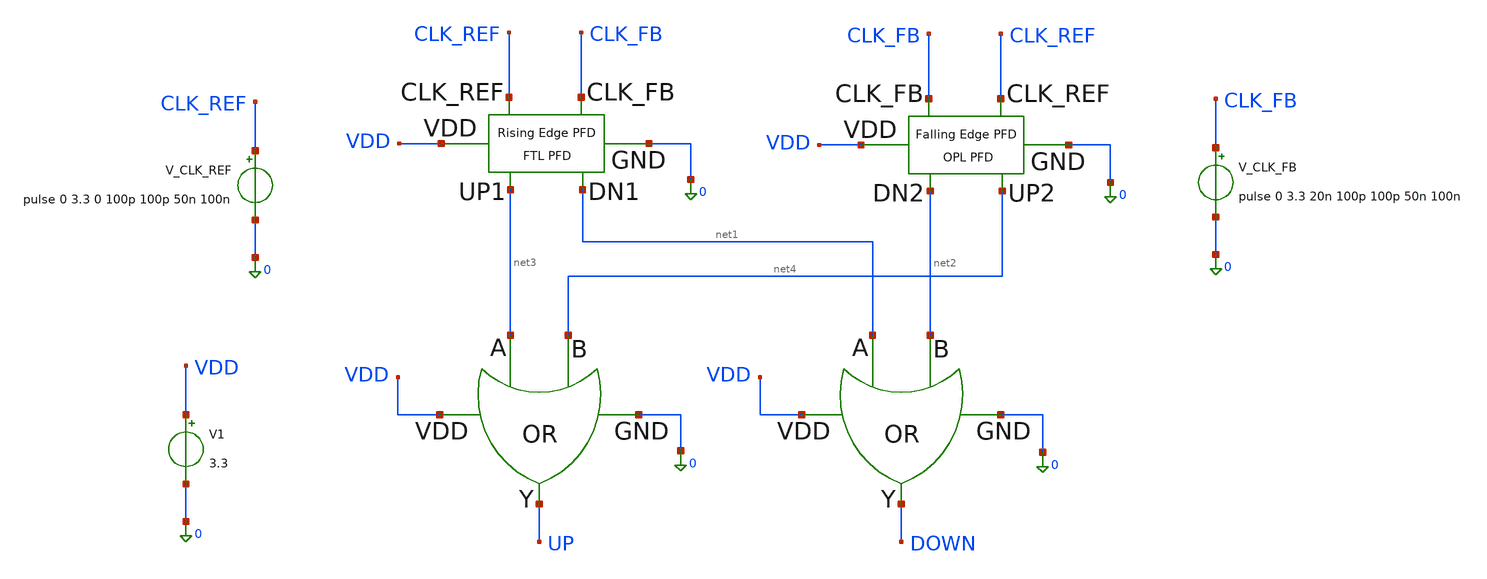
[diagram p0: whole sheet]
** sch_path: PFD/DELD_PFD.sch
**.subckt DELD_PFD
x1 0 net1 net2 VDD DOWN OR
x2 0 net3 net4 VDD UP OR
x3 net1 net3 CLK_FB CLK_REF VDD 0 FTL_PFD
x4 net4 net2 CLK_REF CLK_FB VDD 0 OPL_PFD
V1 VDD 0 3.3
.save i(v1)
V_CLK_REF CLK_REF 0 pulse 0 3.3 0 100p 100p 50n 100n
.save i(v_clk_ref)
V_CLK_FB CLK_FB 0 pulse 0 3.3 20n 100p 100p 50n 100n
.save i(v_clk_fb)
**.ends

* expanding   symbol:  OR.sym # of pins=5
** sym_path: PFD/OR.sym
** sch_path: PFD/OR.sch
.subckt OR GND A B VDD Y
*.opin Y
*.ipin GND
*.ipin VDD
*.ipin A
*.ipin B
XM3 net2 A GND GND nfet_03v3 L=0.28u W=0.22u nf=1 ad='int((nf+1)/2) * W/nf * 0.18u' as='int((nf+2)/2) * W/nf * 0.18u'
+ pd='2*int((nf+1)/2) * (W/nf + 0.18u)' ps='2*int((nf+2)/2) * (W/nf + 0.18u)' nrd='0.18u / W' nrs='0.18u / W'
+ sa=0 sb=0 sd=0 m=1
XM2 net1 A net3 VDD pfet_03v3 L=0.28u W=0.22u nf=1 ad='int((nf+1)/2) * W/nf * 0.18u' as='int((nf+2)/2) * W/nf * 0.18u'
+ pd='2*int((nf+1)/2) * (W/nf + 0.18u)' ps='2*int((nf+2)/2) * (W/nf + 0.18u)' nrd='0.18u / W' nrs='0.18u / W'
+ sa=0 sb=0 sd=0 m=3
XM4 net2 B net1 net4 pfet_03v3 L=0.28u W=0.22u nf=1 ad='int((nf+1)/2) * W/nf * 0.18u' as='int((nf+2)/2) * W/nf * 0.18u'
+ pd='2*int((nf+1)/2) * (W/nf + 0.18u)' ps='2*int((nf+2)/2) * (W/nf + 0.18u)' nrd='0.18u / W' nrs='0.18u / W'
+ sa=0 sb=0 sd=0 m=3
XM1 net2 B GND GND nfet_03v3 L=0.28u W=0.22u nf=1 ad='int((nf+1)/2) * W/nf * 0.18u' as='int((nf+2)/2) * W/nf * 0.18u'
+ pd='2*int((nf+1)/2) * (W/nf + 0.18u)' ps='2*int((nf+2)/2) * (W/nf + 0.18u)' nrd='0.18u / W' nrs='0.18u / W'
+ sa=0 sb=0 sd=0 m=1
XM29 Y net2 VDD VDD pfet_03v3 L=0.28u W=0.22u nf=1 ad='int((nf+1)/2) * W/nf * 0.18u' as='int((nf+2)/2) * W/nf * 0.18u'
+ pd='2*int((nf+1)/2) * (W/nf + 0.18u)' ps='2*int((nf+2)/2) * (W/nf + 0.18u)' nrd='0.18u / W' nrs='0.18u / W'
+ sa=0 sb=0 sd=0 m=3
XM30 Y net2 GND GND nfet_03v3 L=0.28u W=0.22u nf=1 ad='int((nf+1)/2) * W/nf * 0.18u' as='int((nf+2)/2) * W/nf * 0.18u'
+ pd='2*int((nf+1)/2) * (W/nf + 0.18u)' ps='2*int((nf+2)/2) * (W/nf + 0.18u)' nrd='0.18u / W' nrs='0.18u / W'
+ sa=0 sb=0 sd=0 m=1
.ends


* expanding   symbol:  FTL_PFD.sym # of pins=6
** sym_path: PFD/FTL_PFD.sym
** sch_path: PFD/FTL_PFD.sch
.subckt FTL_PFD DN1 UP1 CLK_FB CLK_REF VDD GND
*.opin UP1
*.opin DN1
*.ipin VDD
*.ipin GND
*.ipin CLK_FB
*.ipin CLK_REF
XM1 net1 net3 VDD VDD pfet_03v3 L=0.28u W=0.22u nf=1 ad='int((nf+1)/2) * W/nf * 0.18u' as='int((nf+2)/2) * W/nf * 0.18u'
+ pd='2*int((nf+1)/2) * (W/nf + 0.18u)' ps='2*int((nf+2)/2) * (W/nf + 0.18u)' nrd='0.18u / W' nrs='0.18u / W'
+ sa=0 sb=0 sd=0 m=1
XM4 net2 net3 GND GND nfet_03v3 L=0.28u W=0.22u nf=1 ad='int((nf+1)/2) * W/nf * 0.18u' as='int((nf+2)/2) * W/nf * 0.18u'
+ pd='2*int((nf+1)/2) * (W/nf + 0.18u)' ps='2*int((nf+2)/2) * (W/nf + 0.18u)' nrd='0.18u / W' nrs='0.18u / W'
+ sa=0 sb=0 sd=0 m=1
XM2 net2 CLK_REF net1 VDD pfet_03v3 L=0.28u W=0.22u nf=1 ad='int((nf+1)/2) * W/nf * 0.18u' as='int((nf+2)/2) * W/nf * 0.18u'
+ pd='2*int((nf+1)/2) * (W/nf + 0.18u)' ps='2*int((nf+2)/2) * (W/nf + 0.18u)' nrd='0.18u / W' nrs='0.18u / W'
+ sa=0 sb=0 sd=0 m=1
XM3 net2 CLK_REF GND GND nfet_03v3 L=0.28u W=0.22u nf=1 ad='int((nf+1)/2) * W/nf * 0.18u' as='int((nf+2)/2) * W/nf * 0.18u'
+ pd='2*int((nf+1)/2) * (W/nf + 0.18u)' ps='2*int((nf+2)/2) * (W/nf + 0.18u)' nrd='0.18u / W' nrs='0.18u / W'
+ sa=0 sb=0 sd=0 m=1
XM5 net4 net2 VDD VDD pfet_03v3 L=0.28u W=0.22u nf=1 ad='int((nf+1)/2) * W/nf * 0.18u' as='int((nf+2)/2) * W/nf * 0.18u'
+ pd='2*int((nf+1)/2) * (W/nf + 0.18u)' ps='2*int((nf+2)/2) * (W/nf + 0.18u)' nrd='0.18u / W' nrs='0.18u / W'
+ sa=0 sb=0 sd=0 m=1
XM6 net5 CLK_REF net4 VDD pfet_03v3 L=0.28u W=0.22u nf=1 ad='int((nf+1)/2) * W/nf * 0.18u' as='int((nf+2)/2) * W/nf * 0.18u'
+ pd='2*int((nf+1)/2) * (W/nf + 0.18u)' ps='2*int((nf+2)/2) * (W/nf + 0.18u)' nrd='0.18u / W' nrs='0.18u / W'
+ sa=0 sb=0 sd=0 m=1
XM7 net5 net2 GND GND nfet_03v3 L=0.28u W=0.22u nf=1 ad='int((nf+1)/2) * W/nf * 0.18u' as='int((nf+2)/2) * W/nf * 0.18u'
+ pd='2*int((nf+1)/2) * (W/nf + 0.18u)' ps='2*int((nf+2)/2) * (W/nf + 0.18u)' nrd='0.18u / W' nrs='0.18u / W'
+ sa=0 sb=0 sd=0 m=1
XM9 net6 CLK_REF_bar VDD VDD pfet_03v3 L=0.28u W=0.22u nf=1 ad='int((nf+1)/2) * W/nf * 0.18u' as='int((nf+2)/2) * W/nf * 0.18u'
+ pd='2*int((nf+1)/2) * (W/nf + 0.18u)' ps='2*int((nf+2)/2) * (W/nf + 0.18u)' nrd='0.18u / W' nrs='0.18u / W'
+ sa=0 sb=0 sd=0 m=1
XM10 net7 net5 GND GND nfet_03v3 L=0.28u W=0.22u nf=1 ad='int((nf+1)/2) * W/nf * 0.18u' as='int((nf+2)/2) * W/nf * 0.18u'
+ pd='2*int((nf+1)/2) * (W/nf + 0.18u)' ps='2*int((nf+2)/2) * (W/nf + 0.18u)' nrd='0.18u / W' nrs='0.18u / W'
+ sa=0 sb=0 sd=0 m=1
XM8 net7 net5 net6 VDD pfet_03v3 L=0.28u W=0.22u nf=1 ad='int((nf+1)/2) * W/nf * 0.18u' as='int((nf+2)/2) * W/nf * 0.18u'
+ pd='2*int((nf+1)/2) * (W/nf + 0.18u)' ps='2*int((nf+2)/2) * (W/nf + 0.18u)' nrd='0.18u / W' nrs='0.18u / W'
+ sa=0 sb=0 sd=0 m=1
XM11 net7 CLK_REF_bar GND GND nfet_03v3 L=0.28u W=0.22u nf=1 ad='int((nf+1)/2) * W/nf * 0.18u' as='int((nf+2)/2) * W/nf * 0.18u'
+ pd='2*int((nf+1)/2) * (W/nf + 0.18u)' ps='2*int((nf+2)/2) * (W/nf + 0.18u)' nrd='0.18u / W' nrs='0.18u / W'
+ sa=0 sb=0 sd=0 m=1
XM12 net8 net7 VDD VDD pfet_03v3 L=0.28u W=0.22u nf=1 ad='int((nf+1)/2) * W/nf * 0.18u' as='int((nf+2)/2) * W/nf * 0.18u'
+ pd='2*int((nf+1)/2) * (W/nf + 0.18u)' ps='2*int((nf+2)/2) * (W/nf + 0.18u)' nrd='0.18u / W' nrs='0.18u / W'
+ sa=0 sb=0 sd=0 m=1
XM13 UP1 CLK_REF_bar net8 VDD pfet_03v3 L=0.28u W=0.22u nf=1 ad='int((nf+1)/2) * W/nf * 0.18u' as='int((nf+2)/2) * W/nf * 0.18u'
+ pd='2*int((nf+1)/2) * (W/nf + 0.18u)' ps='2*int((nf+2)/2) * (W/nf + 0.18u)' nrd='0.18u / W' nrs='0.18u / W'
+ sa=0 sb=0 sd=0 m=1
XM14 UP1 net7 GND GND nfet_03v3 L=0.28u W=0.22u nf=1 ad='int((nf+1)/2) * W/nf * 0.18u' as='int((nf+2)/2) * W/nf * 0.18u'
+ pd='2*int((nf+1)/2) * (W/nf + 0.18u)' ps='2*int((nf+2)/2) * (W/nf + 0.18u)' nrd='0.18u / W' nrs='0.18u / W'
+ sa=0 sb=0 sd=0 m=1
XM15 net9 net3 VDD VDD pfet_03v3 L=0.28u W=0.22u nf=1 ad='int((nf+1)/2) * W/nf * 0.18u' as='int((nf+2)/2) * W/nf * 0.18u'
+ pd='2*int((nf+1)/2) * (W/nf + 0.18u)' ps='2*int((nf+2)/2) * (W/nf + 0.18u)' nrd='0.18u / W' nrs='0.18u / W'
+ sa=0 sb=0 sd=0 m=1
XM16 net10 net3 GND GND nfet_03v3 L=0.28u W=0.22u nf=1 ad='int((nf+1)/2) * W/nf * 0.18u' as='int((nf+2)/2) * W/nf * 0.18u'
+ pd='2*int((nf+1)/2) * (W/nf + 0.18u)' ps='2*int((nf+2)/2) * (W/nf + 0.18u)' nrd='0.18u / W' nrs='0.18u / W'
+ sa=0 sb=0 sd=0 m=1
XM17 net10 CLK_FB net9 VDD pfet_03v3 L=0.28u W=0.22u nf=1 ad='int((nf+1)/2) * W/nf * 0.18u' as='int((nf+2)/2) * W/nf * 0.18u'
+ pd='2*int((nf+1)/2) * (W/nf + 0.18u)' ps='2*int((nf+2)/2) * (W/nf + 0.18u)' nrd='0.18u / W' nrs='0.18u / W'
+ sa=0 sb=0 sd=0 m=1
XM18 net10 CLK_FB GND GND nfet_03v3 L=0.28u W=0.22u nf=1 ad='int((nf+1)/2) * W/nf * 0.18u' as='int((nf+2)/2) * W/nf * 0.18u'
+ pd='2*int((nf+1)/2) * (W/nf + 0.18u)' ps='2*int((nf+2)/2) * (W/nf + 0.18u)' nrd='0.18u / W' nrs='0.18u / W'
+ sa=0 sb=0 sd=0 m=1
XM19 net11 net10 VDD VDD pfet_03v3 L=0.28u W=0.22u nf=1 ad='int((nf+1)/2) * W/nf * 0.18u' as='int((nf+2)/2) * W/nf * 0.18u'
+ pd='2*int((nf+1)/2) * (W/nf + 0.18u)' ps='2*int((nf+2)/2) * (W/nf + 0.18u)' nrd='0.18u / W' nrs='0.18u / W'
+ sa=0 sb=0 sd=0 m=1
XM20 net12 CLK_FB net11 VDD pfet_03v3 L=0.28u W=0.22u nf=1 ad='int((nf+1)/2) * W/nf * 0.18u' as='int((nf+2)/2) * W/nf * 0.18u'
+ pd='2*int((nf+1)/2) * (W/nf + 0.18u)' ps='2*int((nf+2)/2) * (W/nf + 0.18u)' nrd='0.18u / W' nrs='0.18u / W'
+ sa=0 sb=0 sd=0 m=1
XM21 net12 net10 GND GND nfet_03v3 L=0.28u W=0.22u nf=1 ad='int((nf+1)/2) * W/nf * 0.18u' as='int((nf+2)/2) * W/nf * 0.18u'
+ pd='2*int((nf+1)/2) * (W/nf + 0.18u)' ps='2*int((nf+2)/2) * (W/nf + 0.18u)' nrd='0.18u / W' nrs='0.18u / W'
+ sa=0 sb=0 sd=0 m=1
XM22 net13 CLK_FB_bar VDD VDD pfet_03v3 L=0.28u W=0.22u nf=1 ad='int((nf+1)/2) * W/nf * 0.18u' as='int((nf+2)/2) * W/nf * 0.18u'
+ pd='2*int((nf+1)/2) * (W/nf + 0.18u)' ps='2*int((nf+2)/2) * (W/nf + 0.18u)' nrd='0.18u / W' nrs='0.18u / W'
+ sa=0 sb=0 sd=0 m=1
XM23 net14 net12 GND GND nfet_03v3 L=0.28u W=0.22u nf=1 ad='int((nf+1)/2) * W/nf * 0.18u' as='int((nf+2)/2) * W/nf * 0.18u'
+ pd='2*int((nf+1)/2) * (W/nf + 0.18u)' ps='2*int((nf+2)/2) * (W/nf + 0.18u)' nrd='0.18u / W' nrs='0.18u / W'
+ sa=0 sb=0 sd=0 m=1
XM24 net14 net12 net13 VDD pfet_03v3 L=0.28u W=0.22u nf=1 ad='int((nf+1)/2) * W/nf * 0.18u' as='int((nf+2)/2) * W/nf * 0.18u'
+ pd='2*int((nf+1)/2) * (W/nf + 0.18u)' ps='2*int((nf+2)/2) * (W/nf + 0.18u)' nrd='0.18u / W' nrs='0.18u / W'
+ sa=0 sb=0 sd=0 m=1
XM25 net14 CLK_FB_bar GND GND nfet_03v3 L=0.28u W=0.22u nf=1 ad='int((nf+1)/2) * W/nf * 0.18u' as='int((nf+2)/2) * W/nf * 0.18u'
+ pd='2*int((nf+1)/2) * (W/nf + 0.18u)' ps='2*int((nf+2)/2) * (W/nf + 0.18u)' nrd='0.18u / W' nrs='0.18u / W'
+ sa=0 sb=0 sd=0 m=1
XM26 net15 net14 VDD VDD pfet_03v3 L=0.28u W=0.22u nf=1 ad='int((nf+1)/2) * W/nf * 0.18u' as='int((nf+2)/2) * W/nf * 0.18u'
+ pd='2*int((nf+1)/2) * (W/nf + 0.18u)' ps='2*int((nf+2)/2) * (W/nf + 0.18u)' nrd='0.18u / W' nrs='0.18u / W'
+ sa=0 sb=0 sd=0 m=1
XM27 DN1 CLK_FB_bar net15 VDD pfet_03v3 L=0.28u W=0.22u nf=1 ad='int((nf+1)/2) * W/nf * 0.18u' as='int((nf+2)/2) * W/nf * 0.18u'
+ pd='2*int((nf+1)/2) * (W/nf + 0.18u)' ps='2*int((nf+2)/2) * (W/nf + 0.18u)' nrd='0.18u / W' nrs='0.18u / W'
+ sa=0 sb=0 sd=0 m=1
XM28 DN1 net14 GND GND nfet_03v3 L=0.28u W=0.22u nf=1 ad='int((nf+1)/2) * W/nf * 0.18u' as='int((nf+2)/2) * W/nf * 0.18u'
+ pd='2*int((nf+1)/2) * (W/nf + 0.18u)' ps='2*int((nf+2)/2) * (W/nf + 0.18u)' nrd='0.18u / W' nrs='0.18u / W'
+ sa=0 sb=0 sd=0 m=1
x1 GND UP1 DN1 VDD net3 XNOR
XM29 CLK_FB_bar CLK_FB VDD VDD pfet_03v3 L=0.28u W=0.22u nf=1 ad='int((nf+1)/2) * W/nf * 0.18u' as='int((nf+2)/2) * W/nf * 0.18u'
+ pd='2*int((nf+1)/2) * (W/nf + 0.18u)' ps='2*int((nf+2)/2) * (W/nf + 0.18u)' nrd='0.18u / W' nrs='0.18u / W'
+ sa=0 sb=0 sd=0 m=3
XM30 CLK_FB_bar CLK_FB GND GND nfet_03v3 L=0.28u W=0.22u nf=1 ad='int((nf+1)/2) * W/nf * 0.18u' as='int((nf+2)/2) * W/nf * 0.18u'
+ pd='2*int((nf+1)/2) * (W/nf + 0.18u)' ps='2*int((nf+2)/2) * (W/nf + 0.18u)' nrd='0.18u / W' nrs='0.18u / W'
+ sa=0 sb=0 sd=0 m=1
XM31 CLK_REF_bar CLK_REF VDD VDD pfet_03v3 L=0.28u W=0.22u nf=1 ad='int((nf+1)/2) * W/nf * 0.18u' as='int((nf+2)/2) * W/nf * 0.18u'
+ pd='2*int((nf+1)/2) * (W/nf + 0.18u)' ps='2*int((nf+2)/2) * (W/nf + 0.18u)' nrd='0.18u / W' nrs='0.18u / W'
+ sa=0 sb=0 sd=0 m=3
XM32 CLK_REF_bar CLK_REF GND GND nfet_03v3 L=0.28u W=0.22u nf=1 ad='int((nf+1)/2) * W/nf * 0.18u' as='int((nf+2)/2) * W/nf * 0.18u'
+ pd='2*int((nf+1)/2) * (W/nf + 0.18u)' ps='2*int((nf+2)/2) * (W/nf + 0.18u)' nrd='0.18u / W' nrs='0.18u / W'
+ sa=0 sb=0 sd=0 m=1
.ends


* expanding   symbol:  OPL_PFD.sym # of pins=6
** sym_path: PFD/OPL_PFD.sym
** sch_path: PFD/OPL_PFD.sch
.subckt OPL_PFD UP2 DN2 CLK_REF CLK_FB VDD GND
*.opin UP2
*.ipin VDD
*.ipin GND
*.ipin CLK_FB
*.ipin CLK_REF
*.opin DN2
XM1 net1 net3 VDD VDD pfet_03v3 L=0.28u W=0.22u nf=1 ad='int((nf+1)/2) * W/nf * 0.18u' as='int((nf+2)/2) * W/nf * 0.18u'
+ pd='2*int((nf+1)/2) * (W/nf + 0.18u)' ps='2*int((nf+2)/2) * (W/nf + 0.18u)' nrd='0.18u / W' nrs='0.18u / W'
+ sa=0 sb=0 sd=0 m=1
XM4 net2 net3 GND GND nfet_03v3 L=0.28u W=0.22u nf=1 ad='int((nf+1)/2) * W/nf * 0.18u' as='int((nf+2)/2) * W/nf * 0.18u'
+ pd='2*int((nf+1)/2) * (W/nf + 0.18u)' ps='2*int((nf+2)/2) * (W/nf + 0.18u)' nrd='0.18u / W' nrs='0.18u / W'
+ sa=0 sb=0 sd=0 m=1
XM5 net4 net1 VDD VDD pfet_03v3 L=0.28u W=0.22u nf=1 ad='int((nf+1)/2) * W/nf * 0.18u' as='int((nf+2)/2) * W/nf * 0.18u'
+ pd='2*int((nf+1)/2) * (W/nf + 0.18u)' ps='2*int((nf+2)/2) * (W/nf + 0.18u)' nrd='0.18u / W' nrs='0.18u / W'
+ sa=0 sb=0 sd=0 m=1
XM7 net5 net1 GND GND nfet_03v3 L=0.28u W=0.22u nf=1 ad='int((nf+1)/2) * W/nf * 0.18u' as='int((nf+2)/2) * W/nf * 0.18u'
+ pd='2*int((nf+1)/2) * (W/nf + 0.18u)' ps='2*int((nf+2)/2) * (W/nf + 0.18u)' nrd='0.18u / W' nrs='0.18u / W'
+ sa=0 sb=0 sd=0 m=1
XM9 net6 CLK_REF_bar net18 VDD pfet_03v3 L=0.28u W=0.22u nf=1 ad='int((nf+1)/2) * W/nf * 0.18u' as='int((nf+2)/2) * W/nf * 0.18u'
+ pd='2*int((nf+1)/2) * (W/nf + 0.18u)' ps='2*int((nf+2)/2) * (W/nf + 0.18u)' nrd='0.18u / W' nrs='0.18u / W'
+ sa=0 sb=0 sd=0 m=1
XM11 net9 CLK_REF_bar GND GND nfet_03v3 L=0.28u W=0.22u nf=1 ad='int((nf+1)/2) * W/nf * 0.18u' as='int((nf+2)/2) * W/nf * 0.18u'
+ pd='2*int((nf+1)/2) * (W/nf + 0.18u)' ps='2*int((nf+2)/2) * (W/nf + 0.18u)' nrd='0.18u / W' nrs='0.18u / W'
+ sa=0 sb=0 sd=0 m=1
XM12 net7 net6 VDD VDD pfet_03v3 L=0.28u W=0.22u nf=1 ad='int((nf+1)/2) * W/nf * 0.18u' as='int((nf+2)/2) * W/nf * 0.18u'
+ pd='2*int((nf+1)/2) * (W/nf + 0.18u)' ps='2*int((nf+2)/2) * (W/nf + 0.18u)' nrd='0.18u / W' nrs='0.18u / W'
+ sa=0 sb=0 sd=0 m=1
XM14 net8 net6 GND GND nfet_03v3 L=0.28u W=0.22u nf=1 ad='int((nf+1)/2) * W/nf * 0.18u' as='int((nf+2)/2) * W/nf * 0.18u'
+ pd='2*int((nf+1)/2) * (W/nf + 0.18u)' ps='2*int((nf+2)/2) * (W/nf + 0.18u)' nrd='0.18u / W' nrs='0.18u / W'
+ sa=0 sb=0 sd=0 m=1
XM2 net1 CLK_REF VDD VDD pfet_03v3 L=0.28u W=0.22u nf=1 ad='int((nf+1)/2) * W/nf * 0.18u' as='int((nf+2)/2) * W/nf * 0.18u'
+ pd='2*int((nf+1)/2) * (W/nf + 0.18u)' ps='2*int((nf+2)/2) * (W/nf + 0.18u)' nrd='0.18u / W' nrs='0.18u / W'
+ sa=0 sb=0 sd=0 m=1
XM6 net4 CLK_REF net5 GND nfet_03v3 L=0.28u W=0.22u nf=1 ad='int((nf+1)/2) * W/nf * 0.18u' as='int((nf+2)/2) * W/nf * 0.18u'
+ pd='2*int((nf+1)/2) * (W/nf + 0.18u)' ps='2*int((nf+2)/2) * (W/nf + 0.18u)' nrd='0.18u / W' nrs='0.18u / W'
+ sa=0 sb=0 sd=0 m=1
XM10 net19 net20 net9 GND nfet_03v3 L=0.28u W=0.22u nf=1 ad='int((nf+1)/2) * W/nf * 0.18u' as='int((nf+2)/2) * W/nf * 0.18u'
+ pd='2*int((nf+1)/2) * (W/nf + 0.18u)' ps='2*int((nf+2)/2) * (W/nf + 0.18u)' nrd='0.18u / W' nrs='0.18u / W'
+ sa=0 sb=0 sd=0 m=1
XM8 net6 net21 VDD VDD pfet_03v3 L=0.28u W=0.22u nf=1 ad='int((nf+1)/2) * W/nf * 0.18u' as='int((nf+2)/2) * W/nf * 0.18u'
+ pd='2*int((nf+1)/2) * (W/nf + 0.18u)' ps='2*int((nf+2)/2) * (W/nf + 0.18u)' nrd='0.18u / W' nrs='0.18u / W'
+ sa=0 sb=0 sd=0 m=1
XM13 net7 CLK_REF_bar net8 GND nfet_03v3 L=0.28u W=0.22u nf=1 ad='int((nf+1)/2) * W/nf * 0.18u' as='int((nf+2)/2) * W/nf * 0.18u'
+ pd='2*int((nf+1)/2) * (W/nf + 0.18u)' ps='2*int((nf+2)/2) * (W/nf + 0.18u)' nrd='0.18u / W' nrs='0.18u / W'
+ sa=0 sb=0 sd=0 m=1
XM15 UP2 net8 VDD VDD pfet_03v3 L=0.28u W=0.22u nf=1 ad='int((nf+1)/2) * W/nf * 0.18u' as='int((nf+2)/2) * W/nf * 0.18u'
+ pd='2*int((nf+1)/2) * (W/nf + 0.18u)' ps='2*int((nf+2)/2) * (W/nf + 0.18u)' nrd='0.18u / W' nrs='0.18u / W'
+ sa=0 sb=0 sd=0 m=3
XM16 UP2 net8 GND GND nfet_03v3 L=0.28u W=0.22u nf=1 ad='int((nf+1)/2) * W/nf * 0.18u' as='int((nf+2)/2) * W/nf * 0.18u'
+ pd='2*int((nf+1)/2) * (W/nf + 0.18u)' ps='2*int((nf+2)/2) * (W/nf + 0.18u)' nrd='0.18u / W' nrs='0.18u / W'
+ sa=0 sb=0 sd=0 m=1
XM17 CLK_FB_bar CLK_FB VDD VDD pfet_03v3 L=0.28u W=0.22u nf=1 ad='int((nf+1)/2) * W/nf * 0.18u' as='int((nf+2)/2) * W/nf * 0.18u'
+ pd='2*int((nf+1)/2) * (W/nf + 0.18u)' ps='2*int((nf+2)/2) * (W/nf + 0.18u)' nrd='0.18u / W' nrs='0.18u / W'
+ sa=0 sb=0 sd=0 m=3
XM18 CLK_FB_bar CLK_FB GND GND nfet_03v3 L=0.28u W=0.22u nf=1 ad='int((nf+1)/2) * W/nf * 0.18u' as='int((nf+2)/2) * W/nf * 0.18u'
+ pd='2*int((nf+1)/2) * (W/nf + 0.18u)' ps='2*int((nf+2)/2) * (W/nf + 0.18u)' nrd='0.18u / W' nrs='0.18u / W'
+ sa=0 sb=0 sd=0 m=1
XM19 CLK_REF_bar CLK_REF VDD VDD pfet_03v3 L=0.28u W=0.22u nf=1 ad='int((nf+1)/2) * W/nf * 0.18u' as='int((nf+2)/2) * W/nf * 0.18u'
+ pd='2*int((nf+1)/2) * (W/nf + 0.18u)' ps='2*int((nf+2)/2) * (W/nf + 0.18u)' nrd='0.18u / W' nrs='0.18u / W'
+ sa=0 sb=0 sd=0 m=3
XM20 CLK_REF_bar CLK_REF GND GND nfet_03v3 L=0.28u W=0.22u nf=1 ad='int((nf+1)/2) * W/nf * 0.18u' as='int((nf+2)/2) * W/nf * 0.18u'
+ pd='2*int((nf+1)/2) * (W/nf + 0.18u)' ps='2*int((nf+2)/2) * (W/nf + 0.18u)' nrd='0.18u / W' nrs='0.18u / W'
+ sa=0 sb=0 sd=0 m=1
XM3 net1 CLK_REF net2 GND nfet_03v3 L=0.28u W=0.22u nf=1 ad='int((nf+1)/2) * W/nf * 0.18u' as='int((nf+2)/2) * W/nf * 0.18u'
+ pd='2*int((nf+1)/2) * (W/nf + 0.18u)' ps='2*int((nf+2)/2) * (W/nf + 0.18u)' nrd='0.18u / W' nrs='0.18u / W'
+ sa=0 sb=0 sd=0 m=1
XM21 net10 net3 VDD VDD pfet_03v3 L=0.28u W=0.22u nf=1 ad='int((nf+1)/2) * W/nf * 0.18u' as='int((nf+2)/2) * W/nf * 0.18u'
+ pd='2*int((nf+1)/2) * (W/nf + 0.18u)' ps='2*int((nf+2)/2) * (W/nf + 0.18u)' nrd='0.18u / W' nrs='0.18u / W'
+ sa=0 sb=0 sd=0 m=1
XM22 net11 net3 GND GND nfet_03v3 L=0.28u W=0.22u nf=1 ad='int((nf+1)/2) * W/nf * 0.18u' as='int((nf+2)/2) * W/nf * 0.18u'
+ pd='2*int((nf+1)/2) * (W/nf + 0.18u)' ps='2*int((nf+2)/2) * (W/nf + 0.18u)' nrd='0.18u / W' nrs='0.18u / W'
+ sa=0 sb=0 sd=0 m=1
XM23 net12 net10 VDD VDD pfet_03v3 L=0.28u W=0.22u nf=1 ad='int((nf+1)/2) * W/nf * 0.18u' as='int((nf+2)/2) * W/nf * 0.18u'
+ pd='2*int((nf+1)/2) * (W/nf + 0.18u)' ps='2*int((nf+2)/2) * (W/nf + 0.18u)' nrd='0.18u / W' nrs='0.18u / W'
+ sa=0 sb=0 sd=0 m=1
XM24 net13 net10 GND GND nfet_03v3 L=0.28u W=0.22u nf=1 ad='int((nf+1)/2) * W/nf * 0.18u' as='int((nf+2)/2) * W/nf * 0.18u'
+ pd='2*int((nf+1)/2) * (W/nf + 0.18u)' ps='2*int((nf+2)/2) * (W/nf + 0.18u)' nrd='0.18u / W' nrs='0.18u / W'
+ sa=0 sb=0 sd=0 m=1
XM25 net14 CLK_FB_bar net22 VDD pfet_03v3 L=0.28u W=0.22u nf=1 ad='int((nf+1)/2) * W/nf * 0.18u' as='int((nf+2)/2) * W/nf * 0.18u'
+ pd='2*int((nf+1)/2) * (W/nf + 0.18u)' ps='2*int((nf+2)/2) * (W/nf + 0.18u)' nrd='0.18u / W' nrs='0.18u / W'
+ sa=0 sb=0 sd=0 m=1
XM26 net17 CLK_FB_bar GND GND nfet_03v3 L=0.28u W=0.22u nf=1 ad='int((nf+1)/2) * W/nf * 0.18u' as='int((nf+2)/2) * W/nf * 0.18u'
+ pd='2*int((nf+1)/2) * (W/nf + 0.18u)' ps='2*int((nf+2)/2) * (W/nf + 0.18u)' nrd='0.18u / W' nrs='0.18u / W'
+ sa=0 sb=0 sd=0 m=1
XM27 net15 net14 VDD VDD pfet_03v3 L=0.28u W=0.22u nf=1 ad='int((nf+1)/2) * W/nf * 0.18u' as='int((nf+2)/2) * W/nf * 0.18u'
+ pd='2*int((nf+1)/2) * (W/nf + 0.18u)' ps='2*int((nf+2)/2) * (W/nf + 0.18u)' nrd='0.18u / W' nrs='0.18u / W'
+ sa=0 sb=0 sd=0 m=1
XM28 net16 net14 GND GND nfet_03v3 L=0.28u W=0.22u nf=1 ad='int((nf+1)/2) * W/nf * 0.18u' as='int((nf+2)/2) * W/nf * 0.18u'
+ pd='2*int((nf+1)/2) * (W/nf + 0.18u)' ps='2*int((nf+2)/2) * (W/nf + 0.18u)' nrd='0.18u / W' nrs='0.18u / W'
+ sa=0 sb=0 sd=0 m=1
XM29 net10 CLK_FB VDD VDD pfet_03v3 L=0.28u W=0.22u nf=1 ad='int((nf+1)/2) * W/nf * 0.18u' as='int((nf+2)/2) * W/nf * 0.18u'
+ pd='2*int((nf+1)/2) * (W/nf + 0.18u)' ps='2*int((nf+2)/2) * (W/nf + 0.18u)' nrd='0.18u / W' nrs='0.18u / W'
+ sa=0 sb=0 sd=0 m=1
XM30 net12 CLK_FB net13 GND nfet_03v3 L=0.28u W=0.22u nf=1 ad='int((nf+1)/2) * W/nf * 0.18u' as='int((nf+2)/2) * W/nf * 0.18u'
+ pd='2*int((nf+1)/2) * (W/nf + 0.18u)' ps='2*int((nf+2)/2) * (W/nf + 0.18u)' nrd='0.18u / W' nrs='0.18u / W'
+ sa=0 sb=0 sd=0 m=1
XM31 net23 net24 net17 GND nfet_03v3 L=0.28u W=0.22u nf=1 ad='int((nf+1)/2) * W/nf * 0.18u' as='int((nf+2)/2) * W/nf * 0.18u'
+ pd='2*int((nf+1)/2) * (W/nf + 0.18u)' ps='2*int((nf+2)/2) * (W/nf + 0.18u)' nrd='0.18u / W' nrs='0.18u / W'
+ sa=0 sb=0 sd=0 m=1
XM32 net14 net25 VDD VDD pfet_03v3 L=0.28u W=0.22u nf=1 ad='int((nf+1)/2) * W/nf * 0.18u' as='int((nf+2)/2) * W/nf * 0.18u'
+ pd='2*int((nf+1)/2) * (W/nf + 0.18u)' ps='2*int((nf+2)/2) * (W/nf + 0.18u)' nrd='0.18u / W' nrs='0.18u / W'
+ sa=0 sb=0 sd=0 m=1
XM33 net15 CLK_FB_bar net16 GND nfet_03v3 L=0.28u W=0.22u nf=1 ad='int((nf+1)/2) * W/nf * 0.18u' as='int((nf+2)/2) * W/nf * 0.18u'
+ pd='2*int((nf+1)/2) * (W/nf + 0.18u)' ps='2*int((nf+2)/2) * (W/nf + 0.18u)' nrd='0.18u / W' nrs='0.18u / W'
+ sa=0 sb=0 sd=0 m=1
XM34 DN2 net16 VDD VDD pfet_03v3 L=0.28u W=0.22u nf=1 ad='int((nf+1)/2) * W/nf * 0.18u' as='int((nf+2)/2) * W/nf * 0.18u'
+ pd='2*int((nf+1)/2) * (W/nf + 0.18u)' ps='2*int((nf+2)/2) * (W/nf + 0.18u)' nrd='0.18u / W' nrs='0.18u / W'
+ sa=0 sb=0 sd=0 m=3
XM35 DN2 net16 GND GND nfet_03v3 L=0.28u W=0.22u nf=1 ad='int((nf+1)/2) * W/nf * 0.18u' as='int((nf+2)/2) * W/nf * 0.18u'
+ pd='2*int((nf+1)/2) * (W/nf + 0.18u)' ps='2*int((nf+2)/2) * (W/nf + 0.18u)' nrd='0.18u / W' nrs='0.18u / W'
+ sa=0 sb=0 sd=0 m=1
XM36 net10 CLK_FB net11 GND nfet_03v3 L=0.28u W=0.22u nf=1 ad='int((nf+1)/2) * W/nf * 0.18u' as='int((nf+2)/2) * W/nf * 0.18u'
+ pd='2*int((nf+1)/2) * (W/nf + 0.18u)' ps='2*int((nf+2)/2) * (W/nf + 0.18u)' nrd='0.18u / W' nrs='0.18u / W'
+ sa=0 sb=0 sd=0 m=1
x1 net26 UP2 DN2 net27 net3 NAND
.ends


* expanding   symbol:  XNOR.sym # of pins=5
** sym_path: PFD/XNOR.sym
** sch_path: PFD/XNOR.sch
.subckt XNOR GND A B VDD Y
*.opin Y
*.ipin VDD
*.ipin GND
*.ipin A
*.ipin B
XM1 net1 net5 VDD VDD pfet_03v3 L=0.28u W=0.22u nf=1 ad='int((nf+1)/2) * W/nf * 0.18u' as='int((nf+2)/2) * W/nf * 0.18u'
+ pd='2*int((nf+1)/2) * (W/nf + 0.18u)' ps='2*int((nf+2)/2) * (W/nf + 0.18u)' nrd='0.18u / W' nrs='0.18u / W'
+ sa=0 sb=0 sd=0 m=1
XM2 Y A_bar net1 VDD pfet_03v3 L=0.28u W=0.22u nf=1 ad='int((nf+1)/2) * W/nf * 0.18u' as='int((nf+2)/2) * W/nf * 0.18u'
+ pd='2*int((nf+1)/2) * (W/nf + 0.18u)' ps='2*int((nf+2)/2) * (W/nf + 0.18u)' nrd='0.18u / W' nrs='0.18u / W'
+ sa=0 sb=0 sd=0 m=1
XM3 Y B_bar net2 GND nfet_03v3 L=0.28u W=0.22u nf=1 ad='int((nf+1)/2) * W/nf * 0.18u' as='int((nf+2)/2) * W/nf * 0.18u'
+ pd='2*int((nf+1)/2) * (W/nf + 0.18u)' ps='2*int((nf+2)/2) * (W/nf + 0.18u)' nrd='0.18u / W' nrs='0.18u / W'
+ sa=0 sb=0 sd=0 m=1
XM4 net2 A GND GND nfet_03v3 L=0.28u W=0.22u nf=1 ad='int((nf+1)/2) * W/nf * 0.18u' as='int((nf+2)/2) * W/nf * 0.18u'
+ pd='2*int((nf+1)/2) * (W/nf + 0.18u)' ps='2*int((nf+2)/2) * (W/nf + 0.18u)' nrd='0.18u / W' nrs='0.18u / W'
+ sa=0 sb=0 sd=0 m=1
XM5 net3 B_bar VDD VDD pfet_03v3 L=0.28u W=0.22u nf=1 ad='int((nf+1)/2) * W/nf * 0.18u' as='int((nf+2)/2) * W/nf * 0.18u'
+ pd='2*int((nf+1)/2) * (W/nf + 0.18u)' ps='2*int((nf+2)/2) * (W/nf + 0.18u)' nrd='0.18u / W' nrs='0.18u / W'
+ sa=0 sb=0 sd=0 m=1
XM6 Y B net3 VDD pfet_03v3 L=0.28u W=0.22u nf=1 ad='int((nf+1)/2) * W/nf * 0.18u' as='int((nf+2)/2) * W/nf * 0.18u'
+ pd='2*int((nf+1)/2) * (W/nf + 0.18u)' ps='2*int((nf+2)/2) * (W/nf + 0.18u)' nrd='0.18u / W' nrs='0.18u / W'
+ sa=0 sb=0 sd=0 m=1
XM7 Y A_bar net4 GND nfet_03v3 L=0.28u W=0.22u nf=1 ad='int((nf+1)/2) * W/nf * 0.18u' as='int((nf+2)/2) * W/nf * 0.18u'
+ pd='2*int((nf+1)/2) * (W/nf + 0.18u)' ps='2*int((nf+2)/2) * (W/nf + 0.18u)' nrd='0.18u / W' nrs='0.18u / W'
+ sa=0 sb=0 sd=0 m=1
XM8 net4 B GND GND nfet_03v3 L=0.28u W=0.22u nf=1 ad='int((nf+1)/2) * W/nf * 0.18u' as='int((nf+2)/2) * W/nf * 0.18u'
+ pd='2*int((nf+1)/2) * (W/nf + 0.18u)' ps='2*int((nf+2)/2) * (W/nf + 0.18u)' nrd='0.18u / W' nrs='0.18u / W'
+ sa=0 sb=0 sd=0 m=1
XM9 A_bar A VDD VDD pfet_03v3 L=0.28u W=0.22u nf=1 ad='int((nf+1)/2) * W/nf * 0.18u' as='int((nf+2)/2) * W/nf * 0.18u'
+ pd='2*int((nf+1)/2) * (W/nf + 0.18u)' ps='2*int((nf+2)/2) * (W/nf + 0.18u)' nrd='0.18u / W' nrs='0.18u / W'
+ sa=0 sb=0 sd=0 m=3
XM10 A_bar A GND GND nfet_03v3 L=0.28u W=0.22u nf=1 ad='int((nf+1)/2) * W/nf * 0.18u' as='int((nf+2)/2) * W/nf * 0.18u'
+ pd='2*int((nf+1)/2) * (W/nf + 0.18u)' ps='2*int((nf+2)/2) * (W/nf + 0.18u)' nrd='0.18u / W' nrs='0.18u / W'
+ sa=0 sb=0 sd=0 m=1
XM11 B_bar B VDD VDD pfet_03v3 L=0.28u W=0.22u nf=1 ad='int((nf+1)/2) * W/nf * 0.18u' as='int((nf+2)/2) * W/nf * 0.18u'
+ pd='2*int((nf+1)/2) * (W/nf + 0.18u)' ps='2*int((nf+2)/2) * (W/nf + 0.18u)' nrd='0.18u / W' nrs='0.18u / W'
+ sa=0 sb=0 sd=0 m=3
XM12 B_bar B GND GND nfet_03v3 L=0.28u W=0.22u nf=1 ad='int((nf+1)/2) * W/nf * 0.18u' as='int((nf+2)/2) * W/nf * 0.18u'
+ pd='2*int((nf+1)/2) * (W/nf + 0.18u)' ps='2*int((nf+2)/2) * (W/nf + 0.18u)' nrd='0.18u / W' nrs='0.18u / W'
+ sa=0 sb=0 sd=0 m=1
.ends


* expanding   symbol:  NAND.sym # of pins=5
** sym_path: PFD/NAND.sym
** sch_path: PFD/NAND.sch
.subckt NAND GND A B VDD Y
*.opin Y
*.ipin GND
*.ipin VDD
*.ipin A
*.ipin B
XM1 Y A net2 VDD pfet_03v3 L=0.28u W=0.22u nf=1 ad='int((nf+1)/2) * W/nf * 0.18u' as='int((nf+2)/2) * W/nf * 0.18u'
+ pd='2*int((nf+1)/2) * (W/nf + 0.18u)' ps='2*int((nf+2)/2) * (W/nf + 0.18u)' nrd='0.18u / W' nrs='0.18u / W'
+ sa=0 sb=0 sd=0 m=3
XM3 Y A net1 GND nfet_03v3 L=0.28u W=0.22u nf=1 ad='int((nf+1)/2) * W/nf * 0.18u' as='int((nf+2)/2) * W/nf * 0.18u'
+ pd='2*int((nf+1)/2) * (W/nf + 0.18u)' ps='2*int((nf+2)/2) * (W/nf + 0.18u)' nrd='0.18u / W' nrs='0.18u / W'
+ sa=0 sb=0 sd=0 m=1
XM4 net1 B GND GND nfet_03v3 L=0.28u W=0.22u nf=1 ad='int((nf+1)/2) * W/nf * 0.18u' as='int((nf+2)/2) * W/nf * 0.18u'
+ pd='2*int((nf+1)/2) * (W/nf + 0.18u)' ps='2*int((nf+2)/2) * (W/nf + 0.18u)' nrd='0.18u / W' nrs='0.18u / W'
+ sa=0 sb=0 sd=0 m=1
XM2 Y B net3 VDD pfet_03v3 L=0.28u W=0.22u nf=1 ad='int((nf+1)/2) * W/nf * 0.18u' as='int((nf+2)/2) * W/nf * 0.18u'
+ pd='2*int((nf+1)/2) * (W/nf + 0.18u)' ps='2*int((nf+2)/2) * (W/nf + 0.18u)' nrd='0.18u / W' nrs='0.18u / W'
+ sa=0 sb=0 sd=0 m=3
.ends

.end
